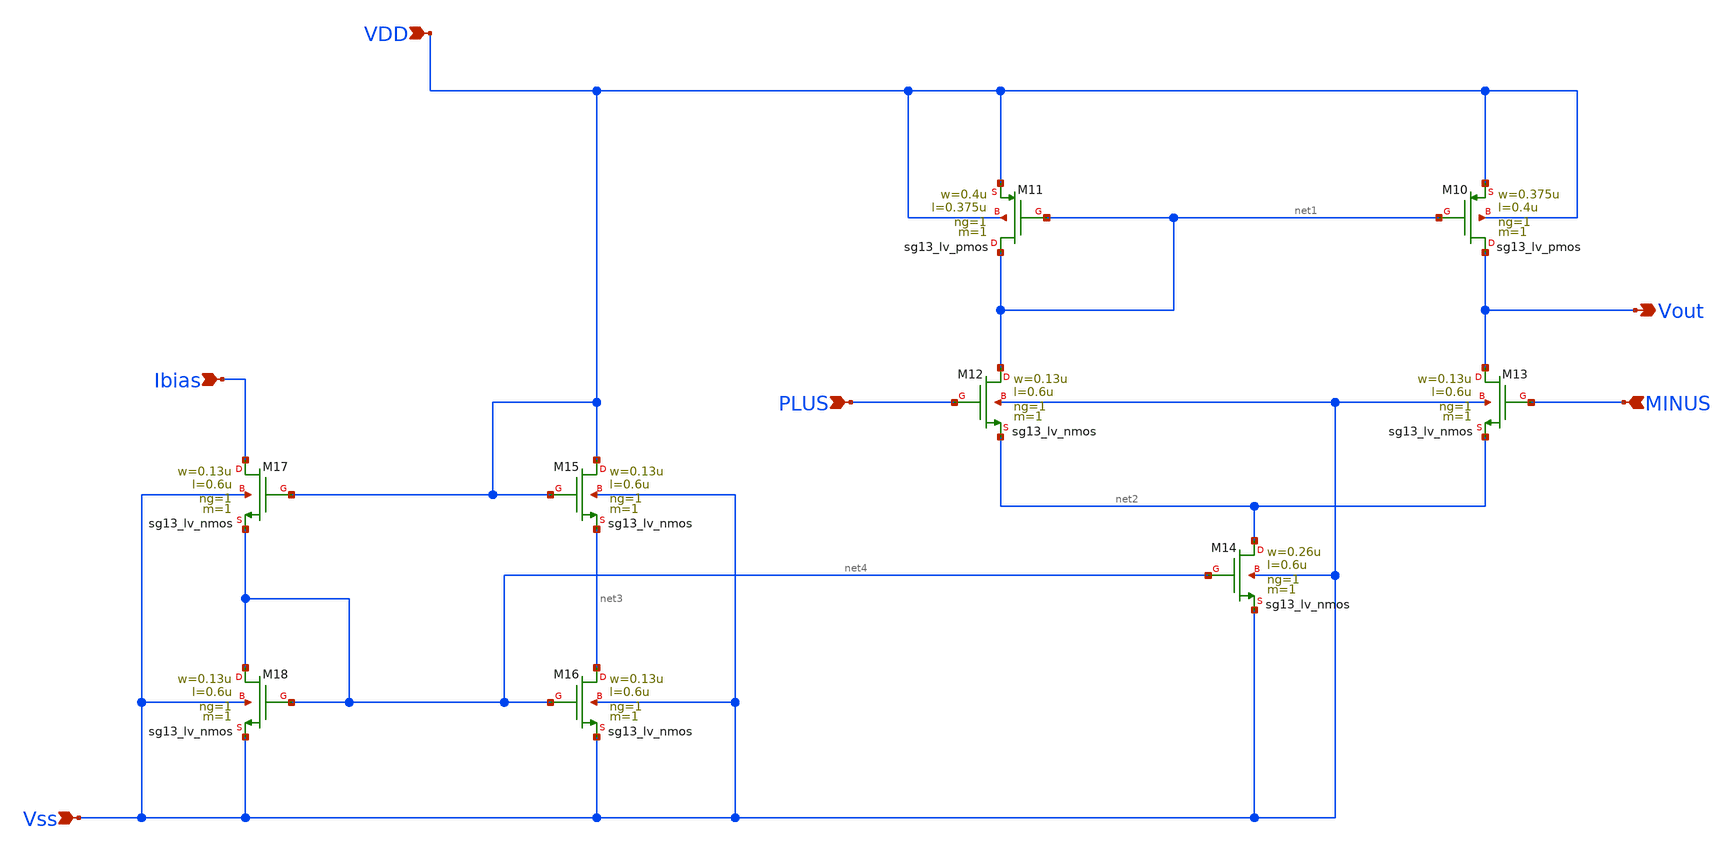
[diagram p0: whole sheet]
** sch_path: DSM/Schematics/IC_Designs_Hrishi/RealCircuits/5-T_OTA/5-T_OTA.sch
* (c) 2024 Hrishikesh, @HSB
**.subckt 5-T_OTA MINUS PLUS VDD Ibias Vss Vout
*.ipin MINUS
*.ipin PLUS
*.ipin VDD
*.ipin Ibias
*.ipin Vss
*.opin Vout
XM10 Vout net1 VDD VDD sg13_lv_pmos w=0.375u l=0.4u ng=1 m=1 mm_ok=1
XM11 net1 net1 VDD VDD sg13_lv_pmos w=0.4u l=0.375u ng=1 m=1 mm_ok=1
XM12 net1 PLUS net2 Vss sg13_lv_nmos w=0.13u l=0.6u ng=1 m=1 mm_ok=1
XM13 Vout MINUS net2 Vss sg13_lv_nmos w=0.13u l=0.6u ng=1 m=1 mm_ok=1
XM14 net2 net4 Vss Vss sg13_lv_nmos w=0.26u l=0.6u ng=1 m=1 mm_ok=1
XM15 VDD VDD net3 Vss sg13_lv_nmos w=0.13u l=0.6u ng=1 m=1 mm_ok=1
XM16 net3 net4 Vss Vss sg13_lv_nmos w=0.13u l=0.6u ng=1 m=1 mm_ok=1
XM17 Ibias VDD net4 Vss sg13_lv_nmos w=0.13u l=0.6u ng=1 m=1 mm_ok=1
XM18 net4 net4 Vss Vss sg13_lv_nmos w=0.13u l=0.6u ng=1 m=1 mm_ok=1
**.ends
.end
